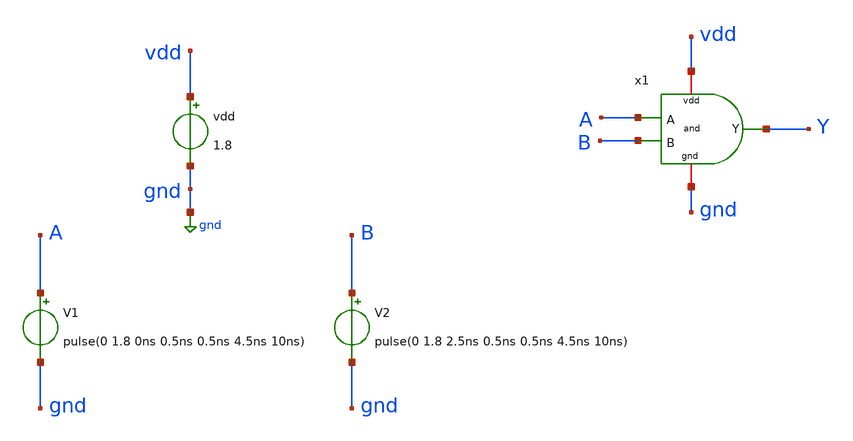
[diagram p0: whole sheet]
** sch_path: LogicGates/and_tb.sch
**.subckt and_tb
x1 vdd gnd A B Y and
vdd vdd gnd 1.8
V1 A gnd pulse(0 1.8 0ns 0.5ns 0.5ns 4.5ns 10ns)
V2 B gnd pulse(0 1.8 2.5ns 0.5ns 0.5ns 4.5ns 10ns)
**** begin user architecture code


.lib /usr/local/share/pdk/sky130A/libs.tech/ngspice/sky130.lib.spice tt
.control
    tran 0.1n 100n
    plot A B
    plot Y
.endc

.save all

**** end user architecture code
**.ends

* expanding   symbol:  LogicGates/and.sym # of pins=5
** sym_path: LogicGates/and.sym
** sch_path: LogicGates/and.sch
.subckt and vdd gnd A B Y
*.ipin A
*.ipin B
*.iopin vdd
*.iopin gnd
*.opin Y
XM1 net1 A net2 gnd sky130_fd_pr__nfet_01v8 L=0.15 W=1 nf=1 ad='int((nf+1)/2) * W/nf * 0.29' as='int((nf+2)/2) * W/nf * 0.29'
+ pd='2*int((nf+1)/2) * (W/nf + 0.29)' ps='2*int((nf+2)/2) * (W/nf + 0.29)' nrd='0.29 / W' nrs='0.29 / W'
+ sa=0 sb=0 sd=0 mult=1 m=1
XM2 net2 B gnd gnd sky130_fd_pr__nfet_01v8 L=0.15 W=1 nf=1 ad='int((nf+1)/2) * W/nf * 0.29' as='int((nf+2)/2) * W/nf * 0.29'
+ pd='2*int((nf+1)/2) * (W/nf + 0.29)' ps='2*int((nf+2)/2) * (W/nf + 0.29)' nrd='0.29 / W' nrs='0.29 / W'
+ sa=0 sb=0 sd=0 mult=1 m=1
XM3 net1 A vdd vdd sky130_fd_pr__pfet_01v8 L=0.15 W=2 nf=1 ad='int((nf+1)/2) * W/nf * 0.29' as='int((nf+2)/2) * W/nf * 0.29'
+ pd='2*int((nf+1)/2) * (W/nf + 0.29)' ps='2*int((nf+2)/2) * (W/nf + 0.29)' nrd='0.29 / W' nrs='0.29 / W'
+ sa=0 sb=0 sd=0 mult=1 m=1
XM4 net1 B vdd vdd sky130_fd_pr__pfet_01v8 L=0.15 W=2 nf=1 ad='int((nf+1)/2) * W/nf * 0.29' as='int((nf+2)/2) * W/nf * 0.29'
+ pd='2*int((nf+1)/2) * (W/nf + 0.29)' ps='2*int((nf+2)/2) * (W/nf + 0.29)' nrd='0.29 / W' nrs='0.29 / W'
+ sa=0 sb=0 sd=0 mult=1 m=1
x1 vdd gnd net1 Y not
.ends


* expanding   symbol:  LogicGates/not.sym # of pins=4
** sym_path: LogicGates/not.sym
** sch_path: LogicGates/not.sch
.subckt not vdd gnd vin vout
*.ipin vin
*.iopin vdd
*.iopin gnd
*.opin vout
XM2 vout vin vdd vdd sky130_fd_pr__pfet_01v8 L=0.15 W=2 nf=1 ad='int((nf+1)/2) * W/nf * 0.29' as='int((nf+2)/2) * W/nf * 0.29'
+ pd='2*int((nf+1)/2) * (W/nf + 0.29)' ps='2*int((nf+2)/2) * (W/nf + 0.29)' nrd='0.29 / W' nrs='0.29 / W'
+ sa=0 sb=0 sd=0 mult=1 m=1
XM1 vout vin gnd gnd sky130_fd_pr__nfet_01v8 L=0.15 W=1 nf=1 ad='int((nf+1)/2) * W/nf * 0.29' as='int((nf+2)/2) * W/nf * 0.29'
+ pd='2*int((nf+1)/2) * (W/nf + 0.29)' ps='2*int((nf+2)/2) * (W/nf + 0.29)' nrd='0.29 / W' nrs='0.29 / W'
+ sa=0 sb=0 sd=0 mult=1 m=1
.ends

.GLOBAL gnd
.end
